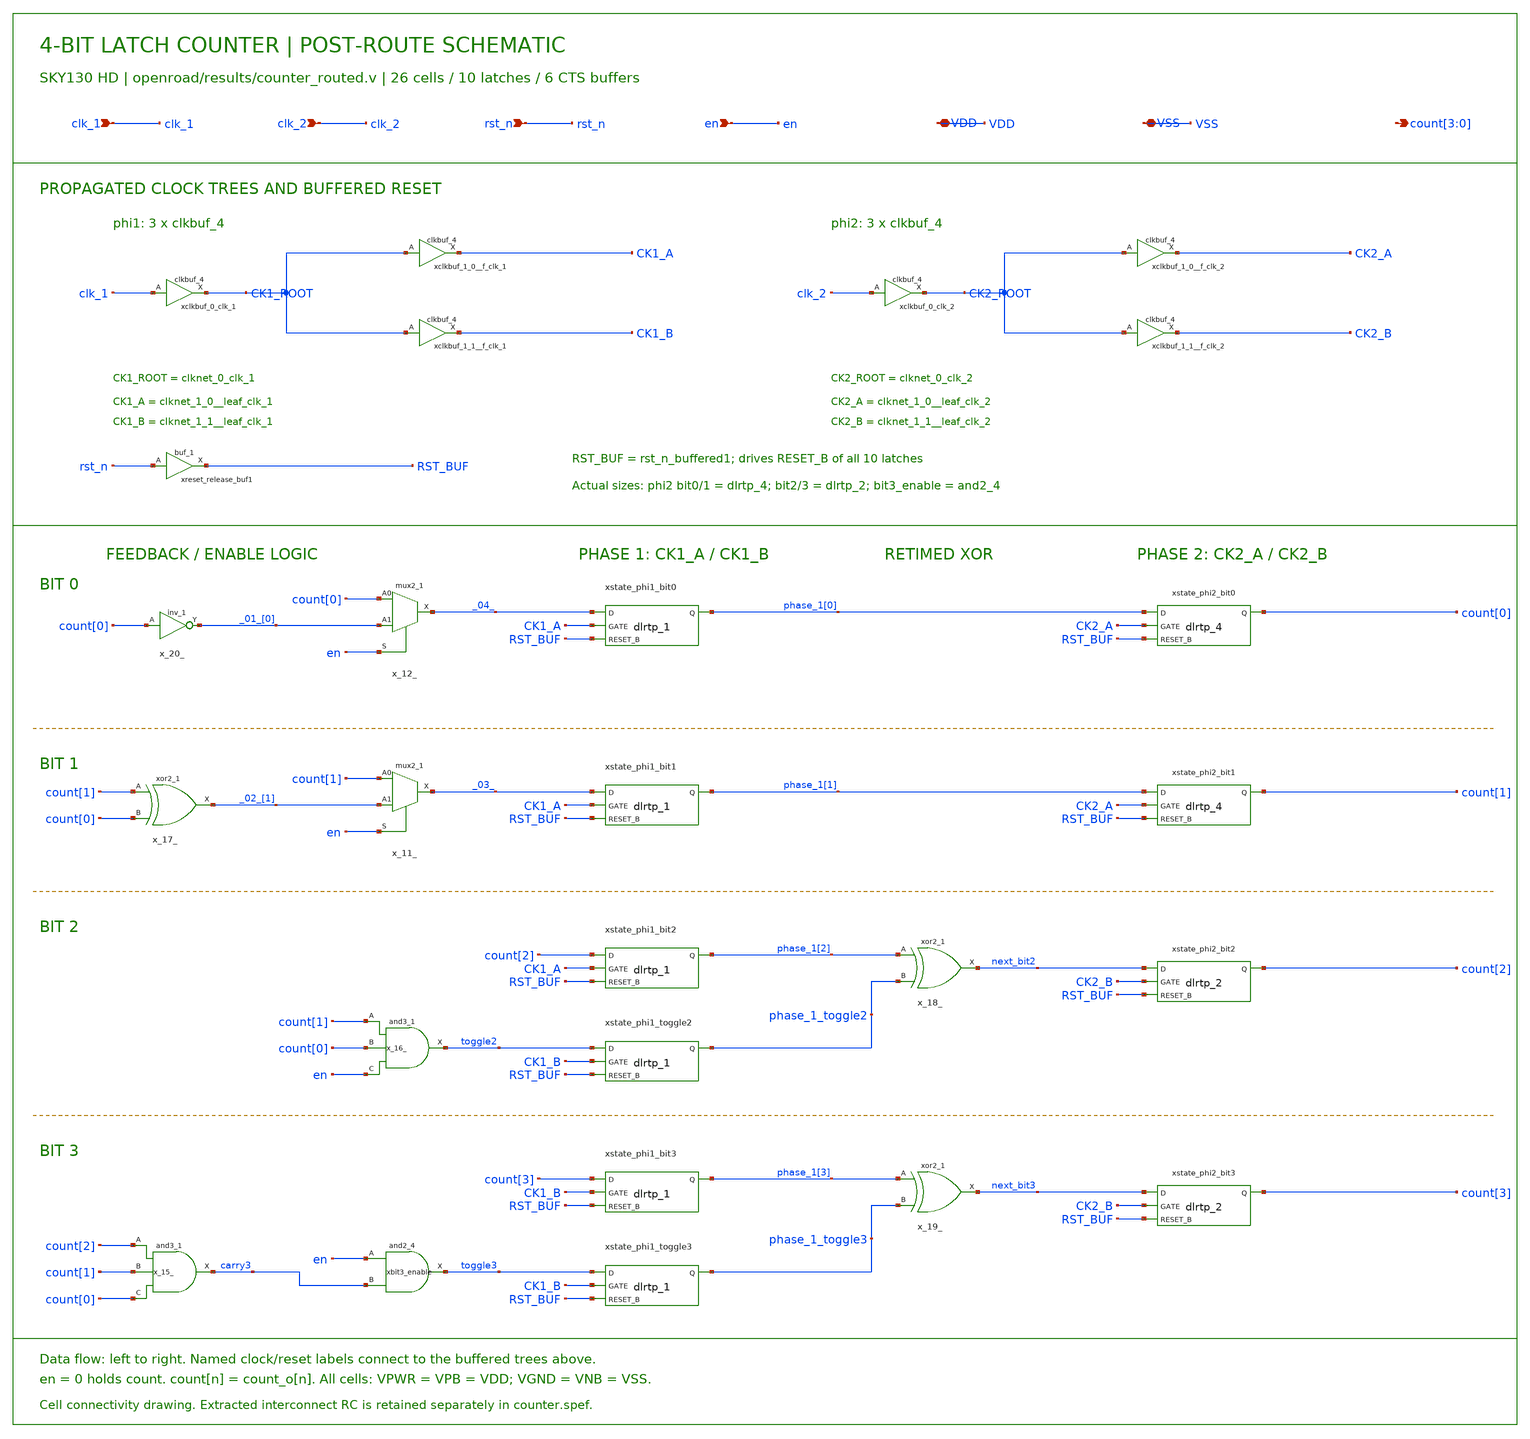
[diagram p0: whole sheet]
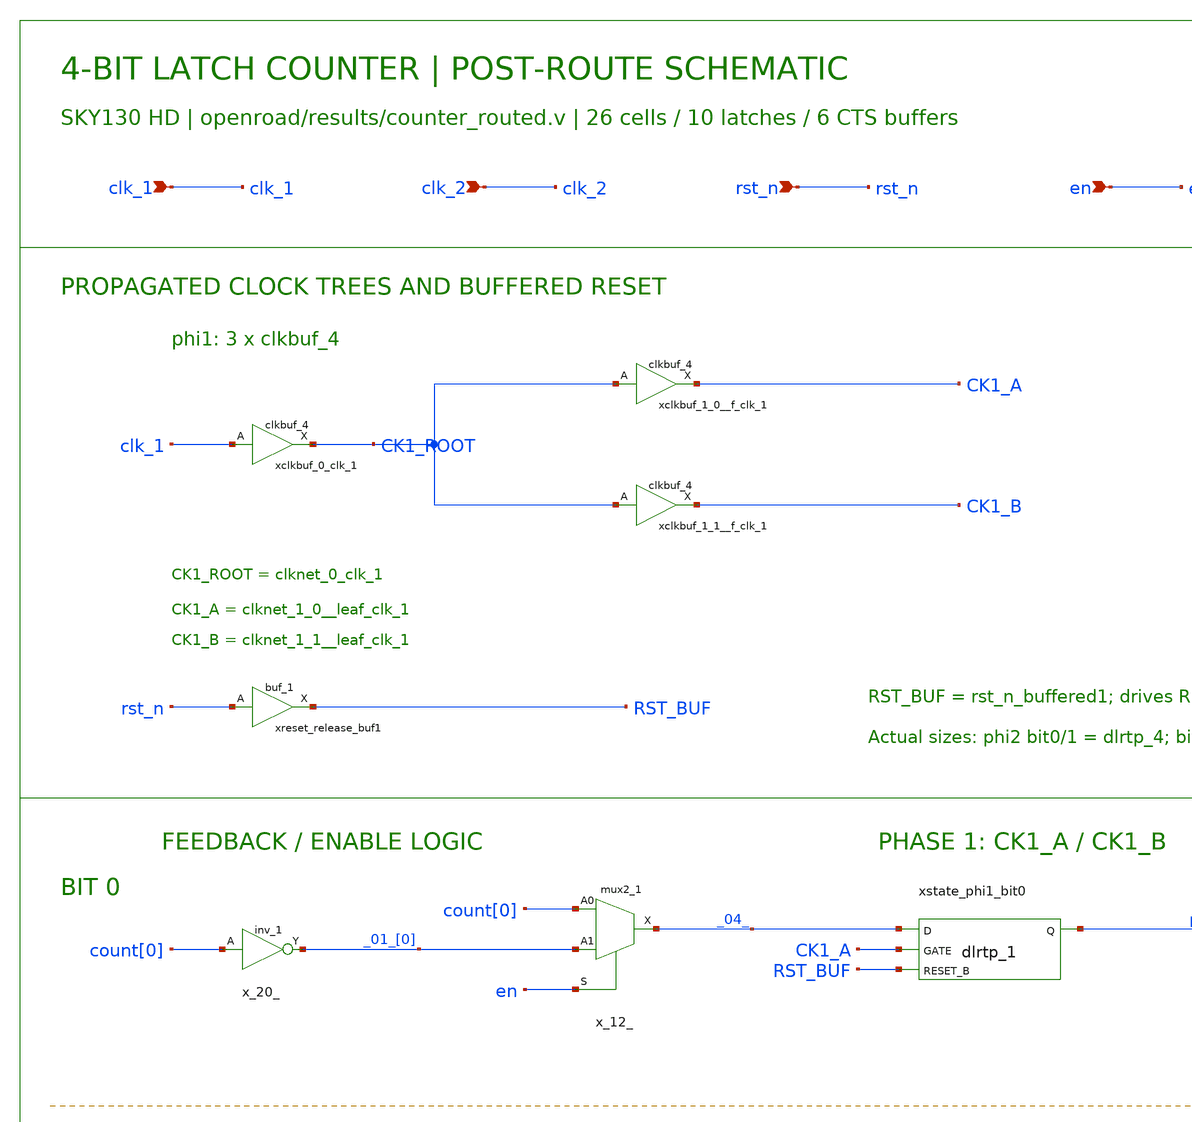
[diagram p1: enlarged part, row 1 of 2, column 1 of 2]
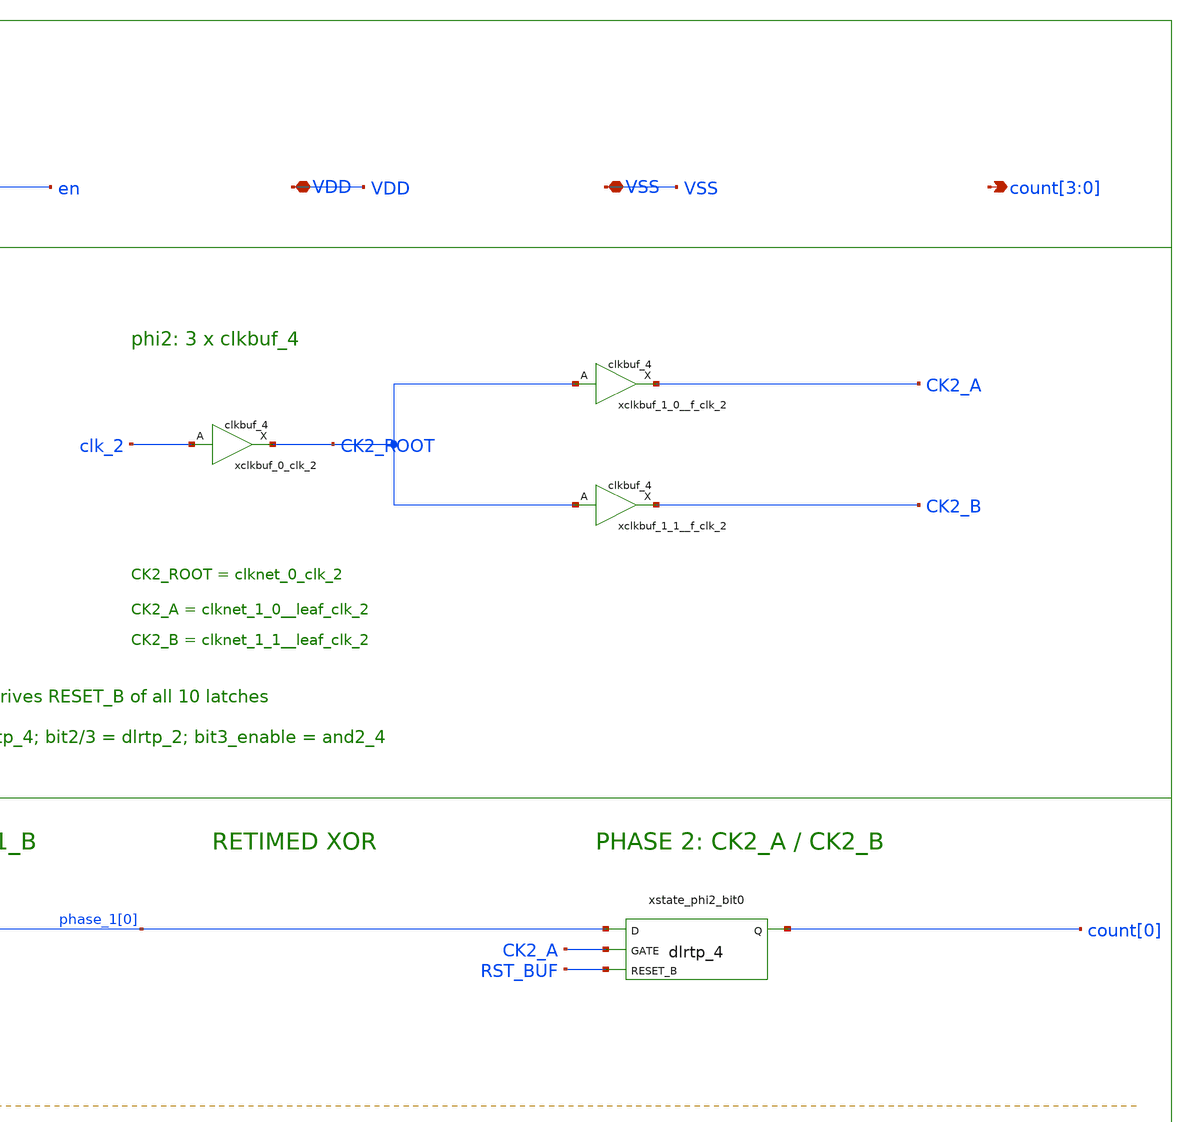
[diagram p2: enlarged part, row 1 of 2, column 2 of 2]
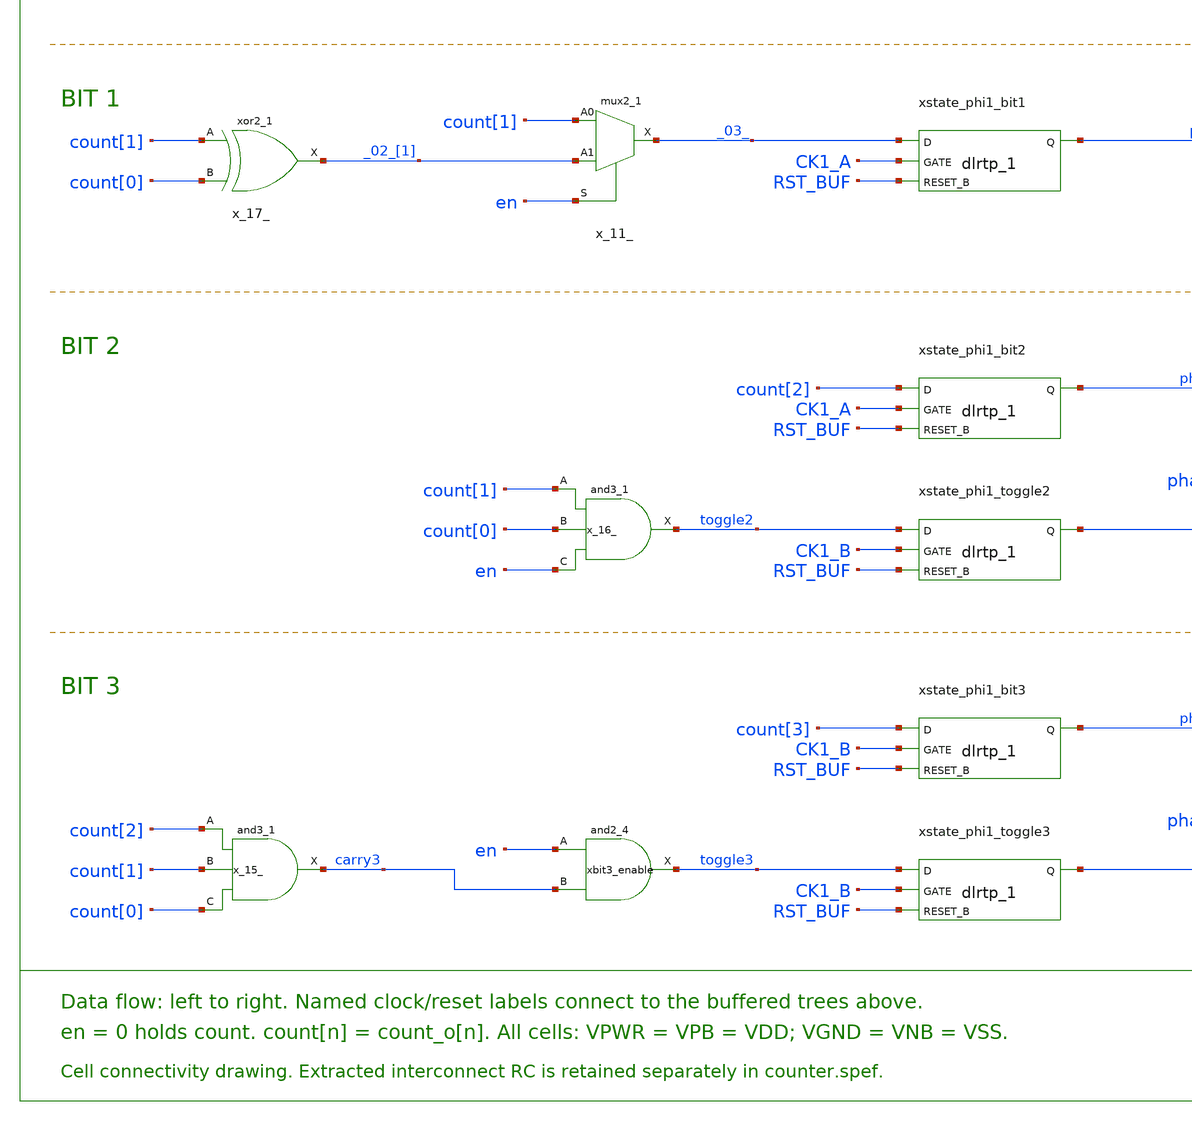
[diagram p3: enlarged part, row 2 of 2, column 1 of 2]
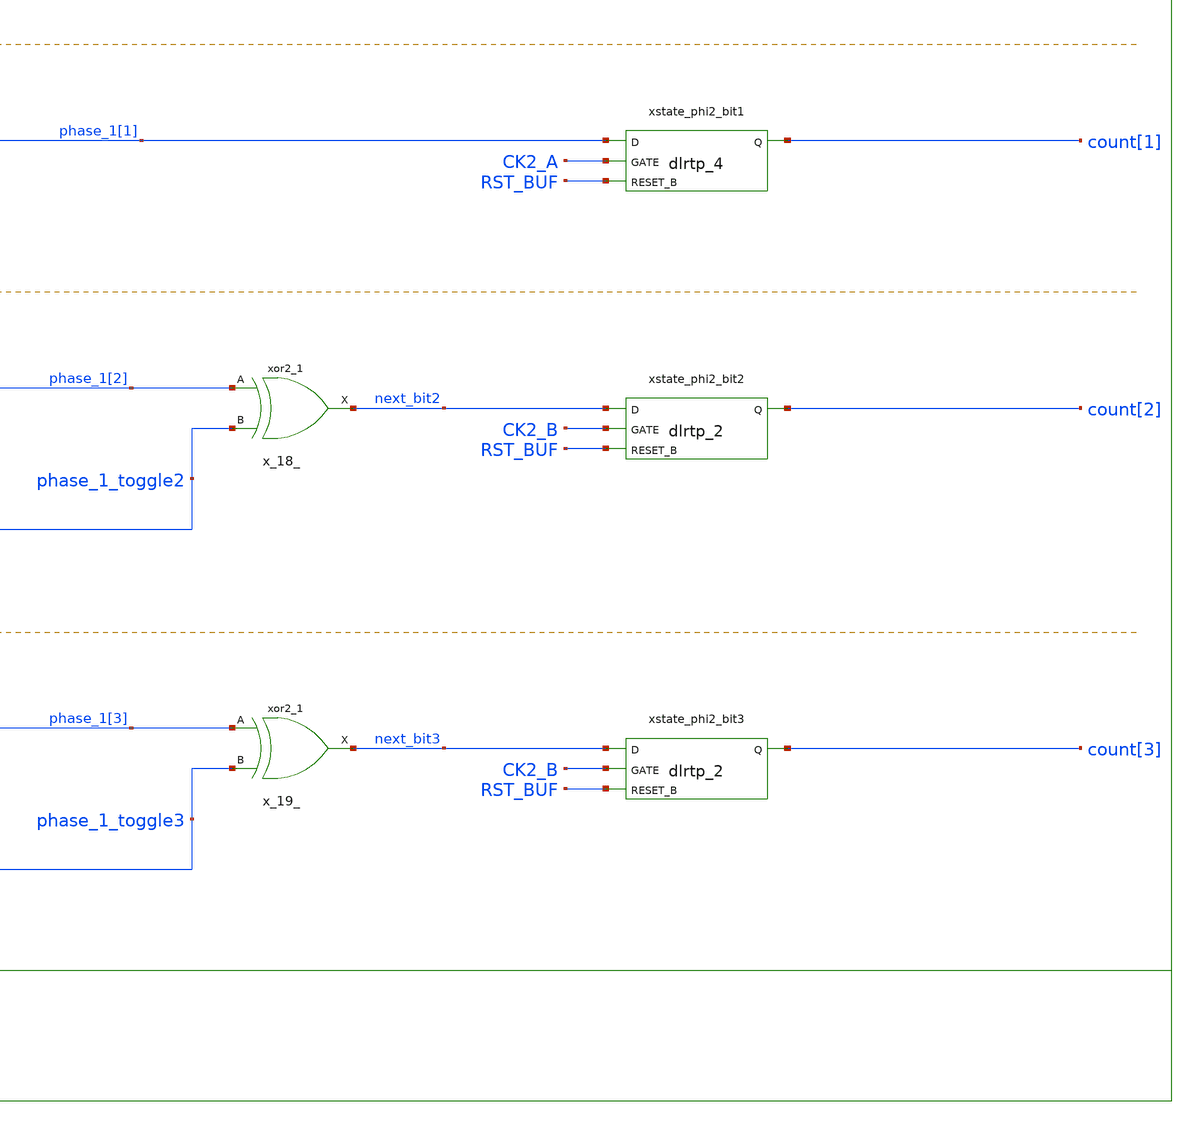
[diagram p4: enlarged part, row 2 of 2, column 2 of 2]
** sch_path: examples/counter/counter_latch_mux_1/counter_postroute.sch
**.subckt counter_postroute clk_1 clk_2 rst_n en VDD VSS count[3],count[2],count[1],count[0]
*.ipin clk_1
*.ipin clk_2
*.ipin rst_n
*.ipin en
*.iopin VDD
*.iopin VSS
*.opin count[3],count[2],count[1],count[0]
xstate_phi1_bit0 _04_ CK1_A RST_BUF VSS VSS VDD VDD phase_1[0] sky130_fd_sc_hd__dlrtp_1
x_12_ count[0] _01_[0] en VSS VSS VDD VDD _04_ sky130_fd_sc_hd__mux2_1
x_20_ count[0] VSS VSS VDD VDD _01_[0] sky130_fd_sc_hd__inv_1
xstate_phi2_bit0 phase_1[0] CK2_A RST_BUF VSS VSS VDD VDD count[0] sky130_fd_sc_hd__dlrtp_4
xstate_phi1_bit1 _03_ CK1_A RST_BUF VSS VSS VDD VDD phase_1[1] sky130_fd_sc_hd__dlrtp_1
x_11_ count[1] _02_[1] en VSS VSS VDD VDD _03_ sky130_fd_sc_hd__mux2_1
x_17_ count[1] count[0] VSS VSS VDD VDD _02_[1] sky130_fd_sc_hd__xor2_1
xstate_phi2_bit1 phase_1[1] CK2_A RST_BUF VSS VSS VDD VDD count[1] sky130_fd_sc_hd__dlrtp_4
xstate_phi1_bit2 count[2] CK1_A RST_BUF VSS VSS VDD VDD phase_1[2] sky130_fd_sc_hd__dlrtp_1
x_18_ phase_1[2] phase_1_toggle2 VSS VSS VDD VDD next_bit2 sky130_fd_sc_hd__xor2_1
xstate_phi2_bit2 next_bit2 CK2_B RST_BUF VSS VSS VDD VDD count[2] sky130_fd_sc_hd__dlrtp_2
xstate_phi1_toggle2 toggle2 CK1_B RST_BUF VSS VSS VDD VDD phase_1_toggle2 sky130_fd_sc_hd__dlrtp_1
x_16_ count[1] count[0] en VSS VSS VDD VDD toggle2 sky130_fd_sc_hd__and3_1
xstate_phi1_bit3 count[3] CK1_B RST_BUF VSS VSS VDD VDD phase_1[3] sky130_fd_sc_hd__dlrtp_1
x_19_ phase_1[3] phase_1_toggle3 VSS VSS VDD VDD next_bit3 sky130_fd_sc_hd__xor2_1
xstate_phi2_bit3 next_bit3 CK2_B RST_BUF VSS VSS VDD VDD count[3] sky130_fd_sc_hd__dlrtp_2
xstate_phi1_toggle3 toggle3 CK1_B RST_BUF VSS VSS VDD VDD phase_1_toggle3 sky130_fd_sc_hd__dlrtp_1
x_15_ count[2] count[1] count[0] VSS VSS VDD VDD carry3 sky130_fd_sc_hd__and3_1
xbit3_enable en carry3 VSS VSS VDD VDD toggle3 sky130_fd_sc_hd__and2_4
xclkbuf_0_clk_1 clk_1 VSS VSS VDD VDD CK1_ROOT sky130_fd_sc_hd__clkbuf_4
xclkbuf_1_0__f_clk_1 CK1_ROOT VSS VSS VDD VDD CK1_A sky130_fd_sc_hd__clkbuf_4
xclkbuf_1_1__f_clk_1 CK1_ROOT VSS VSS VDD VDD CK1_B sky130_fd_sc_hd__clkbuf_4
xclkbuf_0_clk_2 clk_2 VSS VSS VDD VDD CK2_ROOT sky130_fd_sc_hd__clkbuf_4
xclkbuf_1_0__f_clk_2 CK2_ROOT VSS VSS VDD VDD CK2_A sky130_fd_sc_hd__clkbuf_4
xclkbuf_1_1__f_clk_2 CK2_ROOT VSS VSS VDD VDD CK2_B sky130_fd_sc_hd__clkbuf_4
xreset_release_buf1 rst_n VSS VSS VDD VDD RST_BUF sky130_fd_sc_hd__buf_1
**.ends
.end
